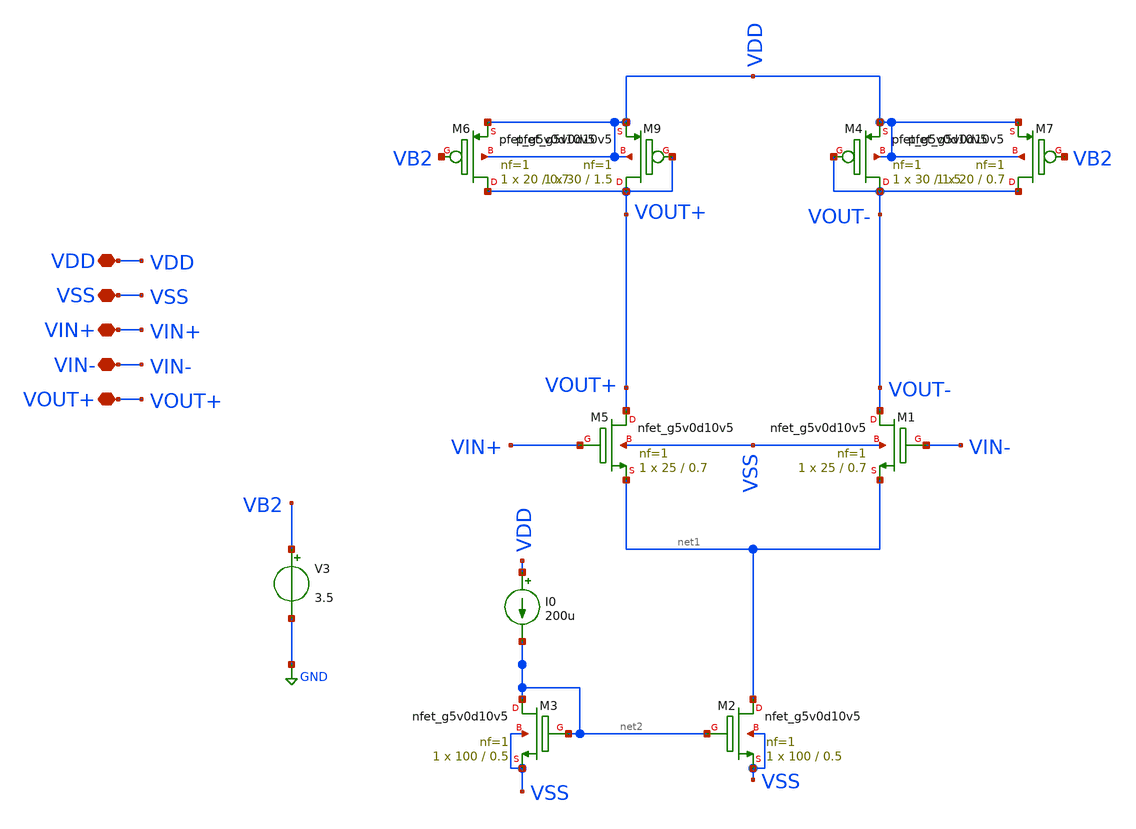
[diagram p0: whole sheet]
** sch_path: amplifiers/differencial_stage_amps/stange stages/dual_load/differential_stage.sch
**.subckt differential_stage VDD VSS VIN+ VIN- VOUT+
*.iopin VDD
*.iopin VSS
*.iopin VIN+
*.iopin VIN-
*.iopin VOUT+
XM5 VOUT+ VIN+ net1 VSS sky130_fd_pr__nfet_g5v0d10v5 L=0.7 W=25 nf=1 ad='int((1 + 1)/2) * 25 / 1 * 0.29'
+ as='int((1 + 2)/2) * 25 / 1 * 0.29' pd='2*int((1 + 1)/2) * (25 / 1 + 0.29)' ps='2*int((1 + 2)/2) * (25 / 1 + 0.29)'
+ nrd='0.29 / 25 ' nrs='0.29 / 25 ' sa=0 sb=0 sd=0 mult=1 m=1
XM1 VOUT- VIN- net1 VSS sky130_fd_pr__nfet_g5v0d10v5 L=0.7 W=25 nf=1 ad='int((1 + 1)/2) * 25 / 1 * 0.29'
+ as='int((1 + 2)/2) * 25 / 1 * 0.29' pd='2*int((1 + 1)/2) * (25 / 1 + 0.29)' ps='2*int((1 + 2)/2) * (25 / 1 + 0.29)'
+ nrd='0.29 / 25 ' nrs='0.29 / 25 ' sa=0 sb=0 sd=0 mult=1 m=1
XM2 net1 net2 VSS VSS sky130_fd_pr__nfet_g5v0d10v5 L=0.5 W=100 nf=1 ad='int((1 + 1)/2) * 100 / 1 * 0.29'
+ as='int((1 + 2)/2) * 100 / 1 * 0.29' pd='2*int((1 + 1)/2) * (100 / 1 + 0.29)' ps='2*int((1 + 2)/2) * (100 / 1 + 0.29)'
+ nrd='0.29 / 100 ' nrs='0.29 / 100 ' sa=0 sb=0 sd=0 mult=1 m=1
XM3 net2 net2 VSS VSS sky130_fd_pr__nfet_g5v0d10v5 L=0.5 W=100 nf=1 ad='int((1 + 1)/2) * 100 / 1 * 0.29'
+ as='int((1 + 2)/2) * 100 / 1 * 0.29' pd='2*int((1 + 1)/2) * (100 / 1 + 0.29)' ps='2*int((1 + 2)/2) * (100 / 1 + 0.29)'
+ nrd='0.29 / 100 ' nrs='0.29 / 100 ' sa=0 sb=0 sd=0 mult=1 m=1
I0 VDD net2 200u
XM9 VOUT+ VOUT+ VDD VDD sky130_fd_pr__pfet_g5v0d10v5 L=1.5 W=30 nf=1 ad='int((1 + 1)/2) * 30 / 1 * 0.29'
+ as='int((1 + 2)/2) * 30 / 1 * 0.29' pd='2*int((1 + 1)/2) * (30 / 1 + 0.29)' ps='2*int((1 + 2)/2) * (30 / 1 + 0.29)'
+ nrd='0.29 / 30 ' nrs='0.29 / 30 ' sa=0 sb=0 sd=0 mult=1 m=1
XM4 VOUT- VOUT- VDD VDD sky130_fd_pr__pfet_g5v0d10v5 L=1.5 W=30 nf=1 ad='int((1 + 1)/2) * 30 / 1 * 0.29'
+ as='int((1 + 2)/2) * 30 / 1 * 0.29' pd='2*int((1 + 1)/2) * (30 / 1 + 0.29)' ps='2*int((1 + 2)/2) * (30 / 1 + 0.29)'
+ nrd='0.29 / 30 ' nrs='0.29 / 30 ' sa=0 sb=0 sd=0 mult=1 m=1
XM6 VOUT+ VB2 VDD VDD sky130_fd_pr__pfet_g5v0d10v5 L=0.7 W=20 nf=1 ad='int((1 + 1)/2) * 20 / 1 * 0.29'
+ as='int((1 + 2)/2) * 20 / 1 * 0.29' pd='2*int((1 + 1)/2) * (20 / 1 + 0.29)' ps='2*int((1 + 2)/2) * (20 / 1 + 0.29)'
+ nrd='0.29 / 20 ' nrs='0.29 / 20 ' sa=0 sb=0 sd=0 mult=1 m=1
XM7 VOUT- VB2 VDD VDD sky130_fd_pr__pfet_g5v0d10v5 L=0.7 W=20 nf=1 ad='int((1 + 1)/2) * 20 / 1 * 0.29'
+ as='int((1 + 2)/2) * 20 / 1 * 0.29' pd='2*int((1 + 1)/2) * (20 / 1 + 0.29)' ps='2*int((1 + 2)/2) * (20 / 1 + 0.29)'
+ nrd='0.29 / 20 ' nrs='0.29 / 20 ' sa=0 sb=0 sd=0 mult=1 m=1
V3 VB2 GND 3.5
**.ends
.GLOBAL GND
.end
